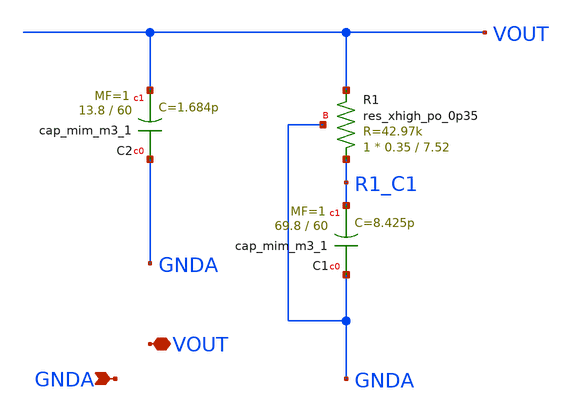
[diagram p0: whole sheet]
** sch_path: projects/pll/charge_pump/xschem_ngspice/loop_filter_xschem.sch
**.subckt loop_filter_xschem GNDA VOUT
*.ipin GNDA
*.iopin VOUT
XC2 GNDA VOUT sky130_fd_pr__cap_mim_m3_1 W=13.8 L=60 MF=1 m=1
XC1 GNDA R1_C1 sky130_fd_pr__cap_mim_m3_1 W=69.8 L=60 MF=1 m=1
XR1 R1_C1 VOUT GNDA sky130_fd_pr__res_xhigh_po_0p35 L=7.52 mult=1 m=1
**.ends
.end
